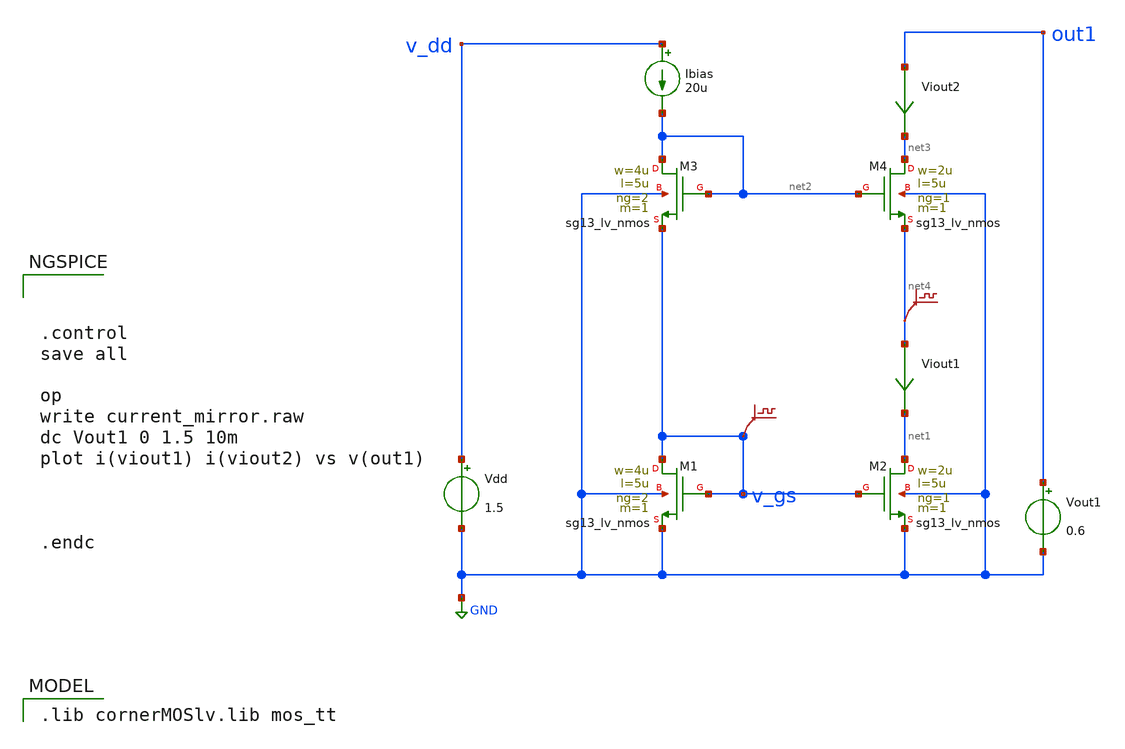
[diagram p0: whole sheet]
** sch_path: Designs/current_mirror/wilsons_current_mirror.sch
* (c) 2025 Thesis_HP, Apache-2.0 license
**.subckt wilsons_current_mirror
Vdd v_dd GND 1.5
XM1 v_gs v_gs GND GND sg13_lv_nmos w=4u l=5u ng=2 m=1 mm_ok=1
Ibias v_dd net2 20u
XM2 net1 v_gs GND GND sg13_lv_nmos w=2u l=5u ng=1 m=1 mm_ok=1
Vout1 out1 GND 0.6
.save v(net4)
.save v(v_gs)
Viout1 net4 net1 0
.save i(viout1)
XM3 net2 net2 v_gs GND sg13_lv_nmos w=4u l=5u ng=2 m=1 mm_ok=1
XM4 net3 net2 net4 GND sg13_lv_nmos w=2u l=5u ng=1 m=1 mm_ok=1
Viout2 out1 net3 0
.save i(viout2)
**** begin user architecture code
 .lib cornerMOSlv.lib mos_tt




.control
save all

op
write current_mirror.raw
dc Vout1 0 1.5 10m
plot i(viout1) i(viout2) vs v(out1)



.endc


**** end user architecture code
**.ends
.GLOBAL GND
.end
